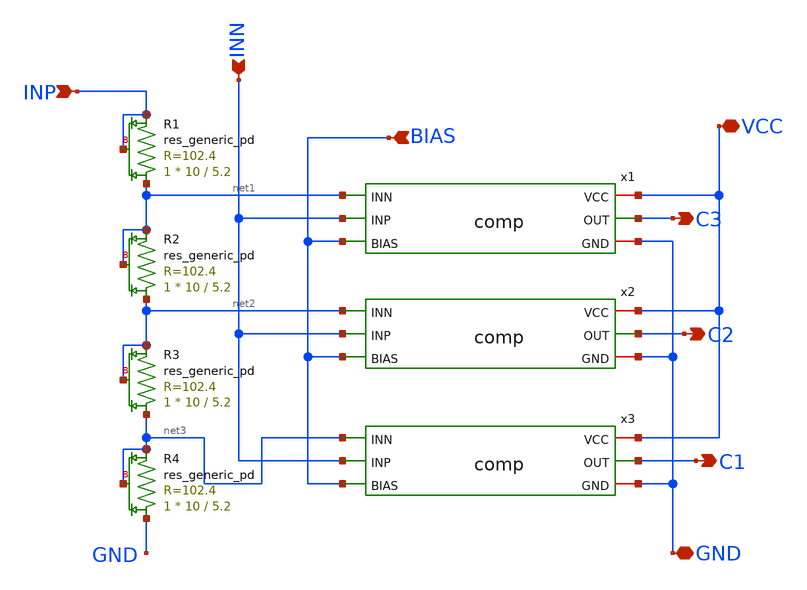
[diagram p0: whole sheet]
** sch_path: week7/pre-layout/Two_BitADC.sch
**.subckt Two_BitADC VCC BIAS C3 C2 C1 INN INP GND
*.iopin VCC
*.ipin BIAS
*.opin C3
*.opin C2
*.opin C1
*.ipin INN
*.ipin INP
*.iopin GND
x1 VCC C3 net1 INN GND BIAS comp
XR1 net1 INP INP sky130_fd_pr__res_generic_pd W=10 L=5.2 mult=1 m=1
XR2 net2 net1 net1 sky130_fd_pr__res_generic_pd W=10 L=5.2 mult=1 m=1
XR3 net3 net2 net2 sky130_fd_pr__res_generic_pd W=10 L=5.2 mult=1 m=1
XR4 GND net3 net3 sky130_fd_pr__res_generic_pd W=10 L=5.2 mult=1 m=1
x2 VCC C2 net2 INN GND BIAS comp
x3 VCC C1 net3 INN GND BIAS comp
**.ends

* expanding   symbol:  comp.sym # of pins=6
** sym_path: week7/pre-layout/comp.sym
** sch_path: week7/pre-layout/comp.sch
.subckt comp VCC OUT INN INP GND BIAS
*.ipin BIAS
*.iopin VCC
*.iopin GND
*.opin OUT
*.ipin INN
*.ipin INP
XM1 net3 net3 VCC VCC sky130_fd_pr__pfet_01v8 L=0.15 W=0.84 nf=1 ad='int((nf+1)/2) * W/nf * 0.29' as='int((nf+2)/2) * W/nf * 0.29'
+ pd='2*int((nf+1)/2) * (W/nf + 0.29)' ps='2*int((nf+2)/2) * (W/nf + 0.29)' nrd='0.29 / W' nrs='0.29 / W'
+ sa=0 sb=0 sd=0 mult=1 m=1
XM3 net3 INN net1 GND sky130_fd_pr__nfet_01v8 L=0.15 W=0.84 nf=1 ad='int((nf+1)/2) * W/nf * 0.29' as='int((nf+2)/2) * W/nf * 0.29'
+ pd='2*int((nf+1)/2) * (W/nf + 0.29)' ps='2*int((nf+2)/2) * (W/nf + 0.29)' nrd='0.29 / W' nrs='0.29 / W'
+ sa=0 sb=0 sd=0 mult=1 m=1
XM12 net1 BIAS GND GND sky130_fd_pr__nfet_01v8 L=0.15 W=0.84 nf=1 ad='int((nf+1)/2) * W/nf * 0.29' as='int((nf+2)/2) * W/nf * 0.29'
+ pd='2*int((nf+1)/2) * (W/nf + 0.29)' ps='2*int((nf+2)/2) * (W/nf + 0.29)' nrd='0.29 / W' nrs='0.29 / W'
+ sa=0 sb=0 sd=0 mult=1 m=1
XM2 net2 net3 VCC VCC sky130_fd_pr__pfet_01v8 L=0.15 W=0.84 nf=1 ad='int((nf+1)/2) * W/nf * 0.29' as='int((nf+2)/2) * W/nf * 0.29'
+ pd='2*int((nf+1)/2) * (W/nf + 0.29)' ps='2*int((nf+2)/2) * (W/nf + 0.29)' nrd='0.29 / W' nrs='0.29 / W'
+ sa=0 sb=0 sd=0 mult=1 m=1
XM4 net2 INP net1 GND sky130_fd_pr__nfet_01v8 L=0.15 W=0.84 nf=1 ad='int((nf+1)/2) * W/nf * 0.29' as='int((nf+2)/2) * W/nf * 0.29'
+ pd='2*int((nf+1)/2) * (W/nf + 0.29)' ps='2*int((nf+2)/2) * (W/nf + 0.29)' nrd='0.29 / W' nrs='0.29 / W'
+ sa=0 sb=0 sd=0 mult=1 m=1
XM5 net4 net2 VCC VCC sky130_fd_pr__pfet_01v8 L=0.15 W=0.84 nf=1 ad='int((nf+1)/2) * W/nf * 0.29' as='int((nf+2)/2) * W/nf * 0.29'
+ pd='2*int((nf+1)/2) * (W/nf + 0.29)' ps='2*int((nf+2)/2) * (W/nf + 0.29)' nrd='0.29 / W' nrs='0.29 / W'
+ sa=0 sb=0 sd=0 mult=1 m=1
XM6 net4 net2 GND GND sky130_fd_pr__nfet_01v8 L=0.15 W=0.84 nf=1 ad='int((nf+1)/2) * W/nf * 0.29' as='int((nf+2)/2) * W/nf * 0.29'
+ pd='2*int((nf+1)/2) * (W/nf + 0.29)' ps='2*int((nf+2)/2) * (W/nf + 0.29)' nrd='0.29 / W' nrs='0.29 / W'
+ sa=0 sb=0 sd=0 mult=1 m=1
XM7 net5 net4 GND GND sky130_fd_pr__nfet_01v8 L=0.15 W=0.84 nf=1 ad='int((nf+1)/2) * W/nf * 0.29' as='int((nf+2)/2) * W/nf * 0.29'
+ pd='2*int((nf+1)/2) * (W/nf + 0.29)' ps='2*int((nf+2)/2) * (W/nf + 0.29)' nrd='0.29 / W' nrs='0.29 / W'
+ sa=0 sb=0 sd=0 mult=1 m=1
XM8 OUT net5 GND GND sky130_fd_pr__nfet_01v8 L=0.15 W=0.84 nf=1 ad='int((nf+1)/2) * W/nf * 0.29' as='int((nf+2)/2) * W/nf * 0.29'
+ pd='2*int((nf+1)/2) * (W/nf + 0.29)' ps='2*int((nf+2)/2) * (W/nf + 0.29)' nrd='0.29 / W' nrs='0.29 / W'
+ sa=0 sb=0 sd=0 mult=1 m=1
XM9 net5 net4 VCC VCC sky130_fd_pr__pfet_01v8 L=0.15 W=0.84 nf=1 ad='int((nf+1)/2) * W/nf * 0.29' as='int((nf+2)/2) * W/nf * 0.29'
+ pd='2*int((nf+1)/2) * (W/nf + 0.29)' ps='2*int((nf+2)/2) * (W/nf + 0.29)' nrd='0.29 / W' nrs='0.29 / W'
+ sa=0 sb=0 sd=0 mult=1 m=1
XM10 OUT net5 VCC VCC sky130_fd_pr__pfet_01v8 L=0.15 W=0.84 nf=1 ad='int((nf+1)/2) * W/nf * 0.29' as='int((nf+2)/2) * W/nf * 0.29'
+ pd='2*int((nf+1)/2) * (W/nf + 0.29)' ps='2*int((nf+2)/2) * (W/nf + 0.29)' nrd='0.29 / W' nrs='0.29 / W'
+ sa=0 sb=0 sd=0 mult=1 m=1
.ends

.end
